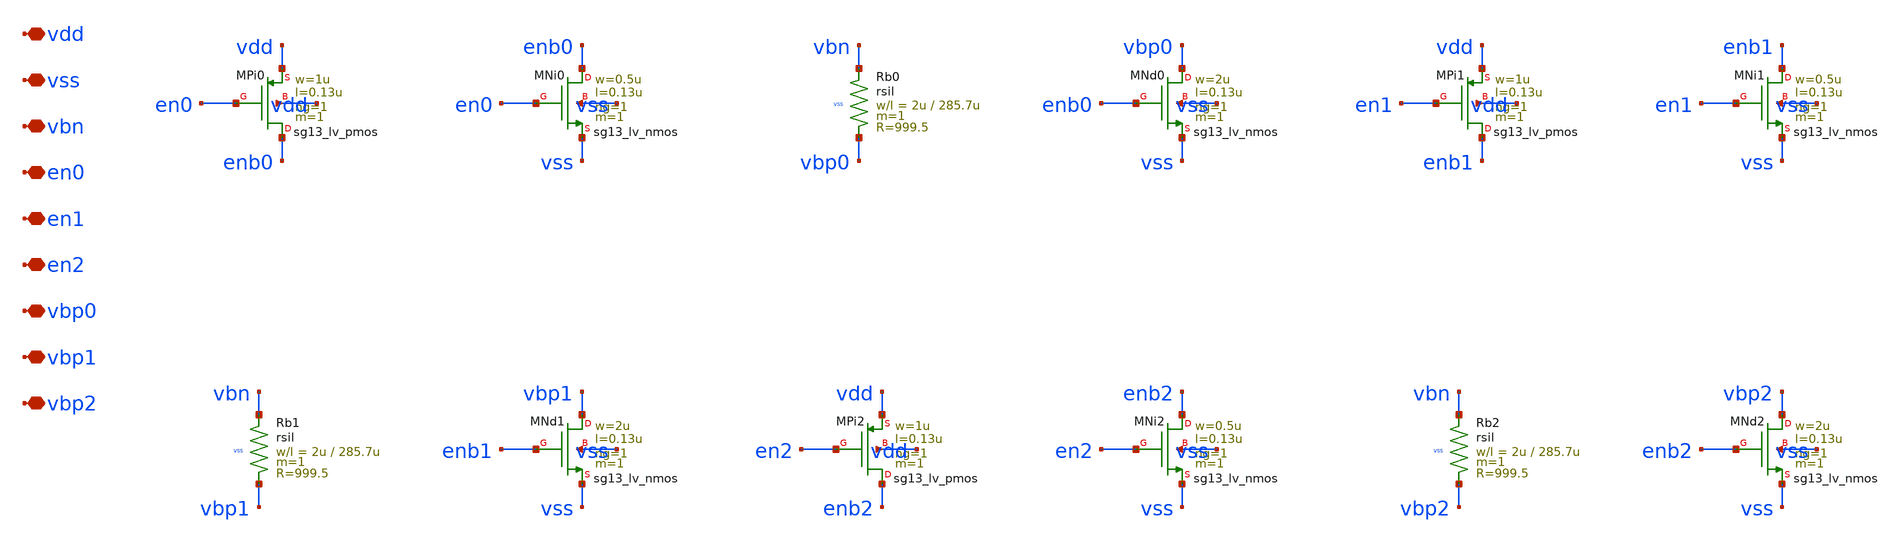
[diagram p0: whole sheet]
** sch_path: design/tx/ffe_en.sch
**.subckt ffe_en vdd vss vbn en0 en1 en2 vbp0 vbp1 vbp2
*.iopin vdd
*.iopin vss
*.iopin vbn
*.iopin en0
*.iopin en1
*.iopin en2
*.iopin vbp0
*.iopin vbp1
*.iopin vbp2
XMPi0 enb0 en0 vdd vdd sg13_lv_pmos w=1u l=0.13u ng=1 m=1 mm_ok=1
XMNi0 enb0 en0 vss vss sg13_lv_nmos w=0.5u l=0.13u ng=1 m=1 mm_ok=1
XRb0 vbn vbp0 vss rsil w=2u l=285.7u m=1 mm_ok=1
XMNd0 vbp0 enb0 vss vss sg13_lv_nmos w=2u l=0.13u ng=1 m=1 mm_ok=1
XMPi1 enb1 en1 vdd vdd sg13_lv_pmos w=1u l=0.13u ng=1 m=1 mm_ok=1
XMNi1 enb1 en1 vss vss sg13_lv_nmos w=0.5u l=0.13u ng=1 m=1 mm_ok=1
XRb1 vbn vbp1 vss rsil w=2u l=285.7u m=1 mm_ok=1
XMNd1 vbp1 enb1 vss vss sg13_lv_nmos w=2u l=0.13u ng=1 m=1 mm_ok=1
XMPi2 enb2 en2 vdd vdd sg13_lv_pmos w=1u l=0.13u ng=1 m=1 mm_ok=1
XMNi2 enb2 en2 vss vss sg13_lv_nmos w=0.5u l=0.13u ng=1 m=1 mm_ok=1
XRb2 vbn vbp2 vss rsil w=2u l=285.7u m=1 mm_ok=1
XMNd2 vbp2 enb2 vss vss sg13_lv_nmos w=2u l=0.13u ng=1 m=1 mm_ok=1
**.ends
.end
